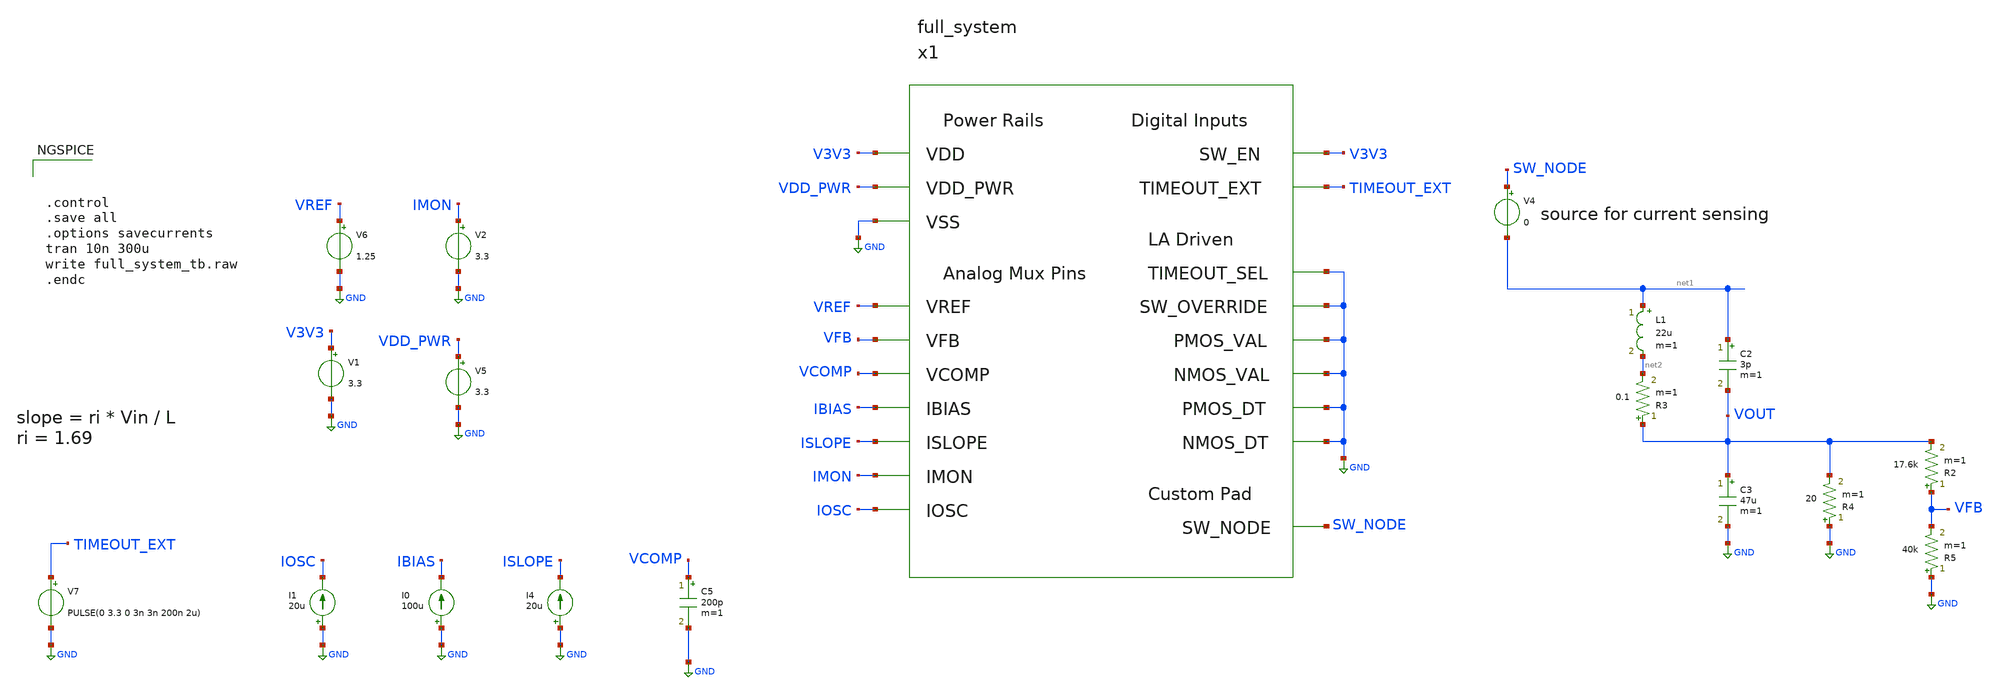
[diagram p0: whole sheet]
** sch_path: design/system/full_system_tb.sch
**.subckt full_system_tb
V1 V3V3 GND 3.3
I0 GND IBIAS 100u
V5 VDD_PWR GND 3.3
V6 VREF GND 1.25
I4 GND ISLOPE 20u
x1 V3V3 VDD_PWR GND VREF VFB VCOMP IBIAS ISLOPE IMON IOSC V3V3 TIMEOUT_EXT GND GND GND GND GND GND
+ SW_NODE full_system
L1 net1 net2 22u m=1
R3 VOUT net2 0.1 m=1
C2 net1 VOUT 3p m=1
C3 VOUT GND 47u m=1
R4 GND VOUT 20 m=1
V4 SW_NODE net1 0
R2 VFB VOUT 17.6k m=1
R5 GND VFB 40k m=1
C5 VCOMP GND 200p m=1
V2 IMON GND 3.3
I1 GND IOSC 20u
V7 TIMEOUT_EXT GND PULSE(0 3.3 0 3n 3n 200n 2u)
**** begin user architecture code



.control
.save all
.options savecurrents
tran 10n 300u
write full_system_tb.raw
.endc



.lib $::SKYWATER_MODELS/models/sky130.lib.spice ff

**** end user architecture code
**.ends
.GLOBAL GND
**** begin user architecture code
[sky130_models]
**** end user architecture code
.end
